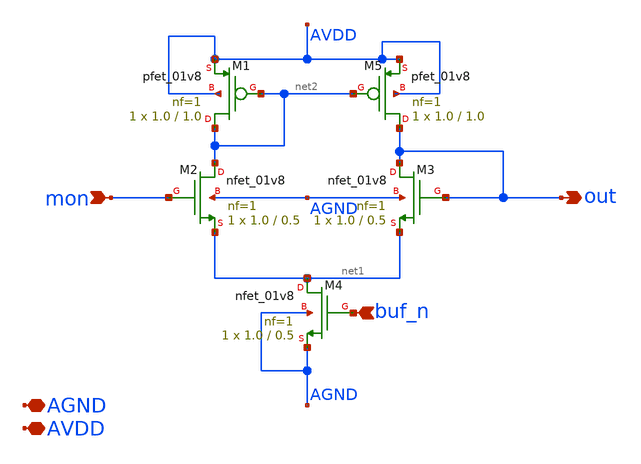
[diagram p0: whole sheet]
** sch_path: design/xschem/buffer_mon.sch
**.subckt buffer_mon AGND AVDD buf_n mon out
*.iopin AGND
*.iopin AVDD
*.ipin buf_n
*.ipin mon
*.opin out
XM1 net2 net2 AVDD AVDD sky130_fd_pr__pfet_01v8 L=1.0 W=1.0 nf=1 ad='int((nf+1)/2) * W/nf * 0.29' as='int((nf+2)/2) * W/nf * 0.29'
+ pd='2*int((nf+1)/2) * (W/nf + 0.29)' ps='2*int((nf+2)/2) * (W/nf + 0.29)' nrd='0.29 / W' nrs='0.29 / W'
+ sa=0 sb=0 sd=0 mult=1 m=1
XM5 out net2 AVDD AVDD sky130_fd_pr__pfet_01v8 L=1.0 W=1.0 nf=1 ad='int((nf+1)/2) * W/nf * 0.29' as='int((nf+2)/2) * W/nf * 0.29'
+ pd='2*int((nf+1)/2) * (W/nf + 0.29)' ps='2*int((nf+2)/2) * (W/nf + 0.29)' nrd='0.29 / W' nrs='0.29 / W'
+ sa=0 sb=0 sd=0 mult=1 m=1
XM4 net1 buf_n AGND AGND sky130_fd_pr__nfet_01v8 L=0.5 W=1.0 nf=1 ad='int((nf+1)/2) * W/nf * 0.29' as='int((nf+2)/2) * W/nf * 0.29'
+ pd='2*int((nf+1)/2) * (W/nf + 0.29)' ps='2*int((nf+2)/2) * (W/nf + 0.29)' nrd='0.29 / W' nrs='0.29 / W'
+ sa=0 sb=0 sd=0 mult=1 m=1
XM2 net2 mon net1 AGND sky130_fd_pr__nfet_01v8 L=0.5 W=1.0 nf=1 ad='int((nf+1)/2) * W/nf * 0.29' as='int((nf+2)/2) * W/nf * 0.29'
+ pd='2*int((nf+1)/2) * (W/nf + 0.29)' ps='2*int((nf+2)/2) * (W/nf + 0.29)' nrd='0.29 / W' nrs='0.29 / W'
+ sa=0 sb=0 sd=0 mult=1 m=1
XM3 out out net1 AGND sky130_fd_pr__nfet_01v8 L=0.5 W=1.0 nf=1 ad='int((nf+1)/2) * W/nf * 0.29' as='int((nf+2)/2) * W/nf * 0.29'
+ pd='2*int((nf+1)/2) * (W/nf + 0.29)' ps='2*int((nf+2)/2) * (W/nf + 0.29)' nrd='0.29 / W' nrs='0.29 / W'
+ sa=0 sb=0 sd=0 mult=1 m=1
**.ends
.end
